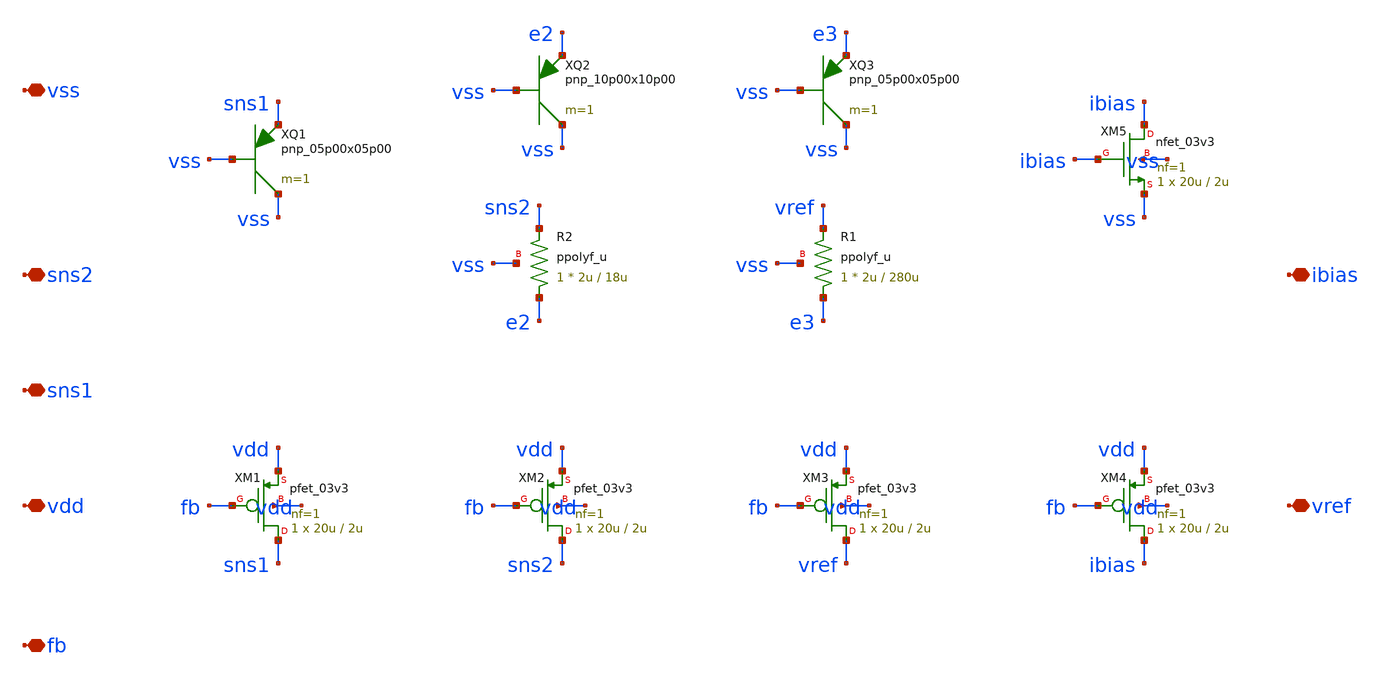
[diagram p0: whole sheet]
** sch_path: design/bandgap_core.sch
**.subckt bandgap_core vdd vss fb sns1 sns2 vref ibias
*.iopin vdd
*.iopin vss
*.iopin fb
*.iopin sns1
*.iopin sns2
*.iopin vref
*.iopin ibias
XM1 sns1 fb vdd vdd pfet_03v3 L=2u W=20u nf=1 ad='int((nf+1)/2) * W/nf * 0.18u' as='int((nf+2)/2) * W/nf * 0.18u'
+ pd='2*int((nf+1)/2) * (W/nf + 0.18u)' ps='2*int((nf+2)/2) * (W/nf + 0.18u)' nrd='0.18u / W' nrs='0.18u / W'
+ sa=0 sb=0 sd=0 m=1
XQ1 vss vss sns1 pnp_05p00x05p00 m=1 par=1
XM2 sns2 fb vdd vdd pfet_03v3 L=2u W=20u nf=1 ad='int((nf+1)/2) * W/nf * 0.18u' as='int((nf+2)/2) * W/nf * 0.18u'
+ pd='2*int((nf+1)/2) * (W/nf + 0.18u)' ps='2*int((nf+2)/2) * (W/nf + 0.18u)' nrd='0.18u / W' nrs='0.18u / W'
+ sa=0 sb=0 sd=0 m=1
XR2 e2 sns2 vss ppolyf_u r_width=2u r_length=18u m=1
XQ2 vss vss e2 pnp_10p00x10p00 m=1
XM3 vref fb vdd vdd pfet_03v3 L=2u W=20u nf=1 ad='int((nf+1)/2) * W/nf * 0.18u' as='int((nf+2)/2) * W/nf * 0.18u'
+ pd='2*int((nf+1)/2) * (W/nf + 0.18u)' ps='2*int((nf+2)/2) * (W/nf + 0.18u)' nrd='0.18u / W' nrs='0.18u / W'
+ sa=0 sb=0 sd=0 m=1
XR1 e3 vref vss ppolyf_u r_width=2u r_length=280u m=1
XQ3 vss vss e3 pnp_05p00x05p00 m=1 par=1
XM4 ibias fb vdd vdd pfet_03v3 L=2u W=20u nf=1 ad='int((nf+1)/2) * W/nf * 0.18u' as='int((nf+2)/2) * W/nf * 0.18u'
+ pd='2*int((nf+1)/2) * (W/nf + 0.18u)' ps='2*int((nf+2)/2) * (W/nf + 0.18u)' nrd='0.18u / W' nrs='0.18u / W'
+ sa=0 sb=0 sd=0 m=1
XM5 ibias ibias vss vss nfet_03v3 L=2u W=20u nf=1 ad='int((nf+1)/2) * W/nf * 0.18u' as='int((nf+2)/2) * W/nf * 0.18u'
+ pd='2*int((nf+1)/2) * (W/nf + 0.18u)' ps='2*int((nf+2)/2) * (W/nf + 0.18u)' nrd='0.18u / W' nrs='0.18u / W'
+ sa=0 sb=0 sd=0 m=1
**.ends
.end
